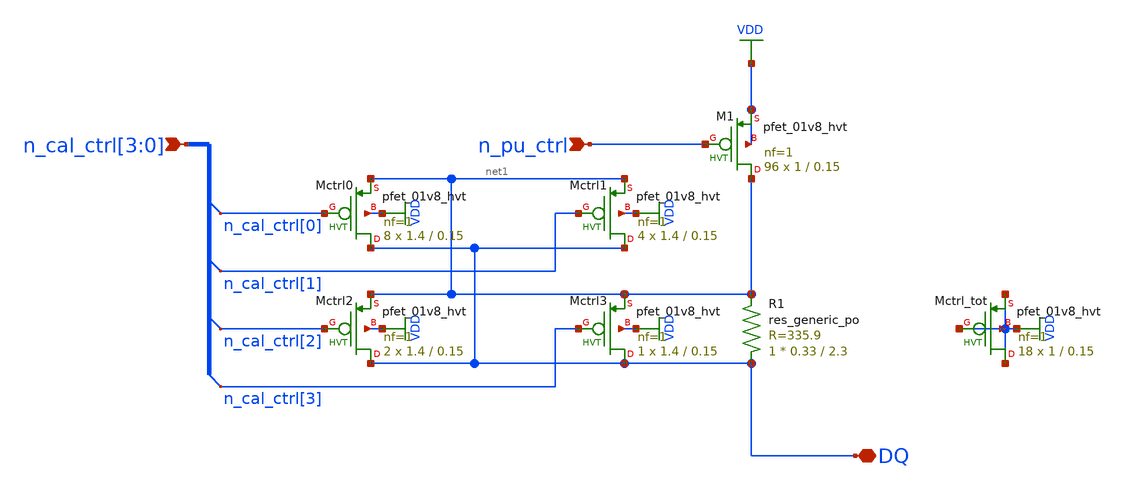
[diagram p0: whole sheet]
** sch_path: p-leg.sch
* Copyright 2021 Stefan Frederik Schippers
* Licensed under the Apache License, Version 2.0 (the "License");
* you may not use this file except in compliance with the License.
* You may obtain a copy of the License at
* https://www.apache.org/licenses/LICENSE-2.0
* Unless required by applicable law or agreed to in writing, software
* distributed under the License is distributed on an "AS IS" BASIS,
* WITHOUT WARRANTIES OR CONDITIONS OF ANY KIND, either express or implied.
* See the License for the specific language governing permissions and
* limitations under the License.
**.subckt p-leg n_cal_ctrl[3],n_cal_ctrl[2],n_cal_ctrl[1],n_cal_ctrl[0] n_pu_ctrl DQ
*.ipin n_cal_ctrl[3],n_cal_ctrl[2],n_cal_ctrl[1],n_cal_ctrl[0]
*.ipin n_pu_ctrl
*.iopin DQ
XM1 net1 n_pu_ctrl VDD VDD sky130_fd_pr__pfet_01v8_hvt L=0.15 W=1 nf=1 ad='int((nf+1)/2) * W/nf * 0.29'
+ as='int((nf+2)/2) * W/nf * 0.29' pd='2*int((nf+1)/2) * (W/nf + 0.29)' ps='2*int((nf+2)/2) * (W/nf + 0.29)'
+ nrd='0.29 / W' nrs='0.29 / W' sa=0 sb=0 sd=0 mult=96 m=96
XR1 DQ net1 sky130_fd_pr__res_generic_po W=0.33 L=2.3 m=1
XMctrl_tot VDD VDD VDD VDD sky130_fd_pr__pfet_01v8_hvt L=0.15 W=1 nf=1 ad='int((nf+1)/2) * W/nf * 0.29'
+ as='int((nf+2)/2) * W/nf * 0.29' pd='2*int((nf+1)/2) * (W/nf + 0.29)' ps='2*int((nf+2)/2) * (W/nf + 0.29)'
+ nrd='0.29 / W' nrs='0.29 / W' sa=0 sb=0 sd=0 mult=18 m=18
XMctrl0 DQ n_cal_ctrl[0] net1 VDD sky130_fd_pr__pfet_01v8_hvt L=0.15 W=1.4 nf=1 ad='int((nf+1)/2) * W/nf * 0.29'
+ as='int((nf+2)/2) * W/nf * 0.29' pd='2*int((nf+1)/2) * (W/nf + 0.29)' ps='2*int((nf+2)/2) * (W/nf + 0.29)'
+ nrd='0.29 / W' nrs='0.29 / W' sa=0 sb=0 sd=0 mult=8 m=8
XMctrl1 DQ n_cal_ctrl[1] net1 VDD sky130_fd_pr__pfet_01v8_hvt L=0.15 W=1.4 nf=1 ad='int((nf+1)/2) * W/nf * 0.29'
+ as='int((nf+2)/2) * W/nf * 0.29' pd='2*int((nf+1)/2) * (W/nf + 0.29)' ps='2*int((nf+2)/2) * (W/nf + 0.29)'
+ nrd='0.29 / W' nrs='0.29 / W' sa=0 sb=0 sd=0 mult=4 m=4
XMctrl2 DQ n_cal_ctrl[2] net1 VDD sky130_fd_pr__pfet_01v8_hvt L=0.15 W=1.4 nf=1 ad='int((nf+1)/2) * W/nf * 0.29'
+ as='int((nf+2)/2) * W/nf * 0.29' pd='2*int((nf+1)/2) * (W/nf + 0.29)' ps='2*int((nf+2)/2) * (W/nf + 0.29)'
+ nrd='0.29 / W' nrs='0.29 / W' sa=0 sb=0 sd=0 mult=2 m=2
XMctrl3 DQ n_cal_ctrl[3] net1 VDD sky130_fd_pr__pfet_01v8_hvt L=0.15 W=1.4 nf=1 ad='int((nf+1)/2) * W/nf * 0.29'
+ as='int((nf+2)/2) * W/nf * 0.29' pd='2*int((nf+1)/2) * (W/nf + 0.29)' ps='2*int((nf+2)/2) * (W/nf + 0.29)'
+ nrd='0.29 / W' nrs='0.29 / W' sa=0 sb=0 sd=0 mult=1 m=1
**.ends
.GLOBAL VDD
.end
